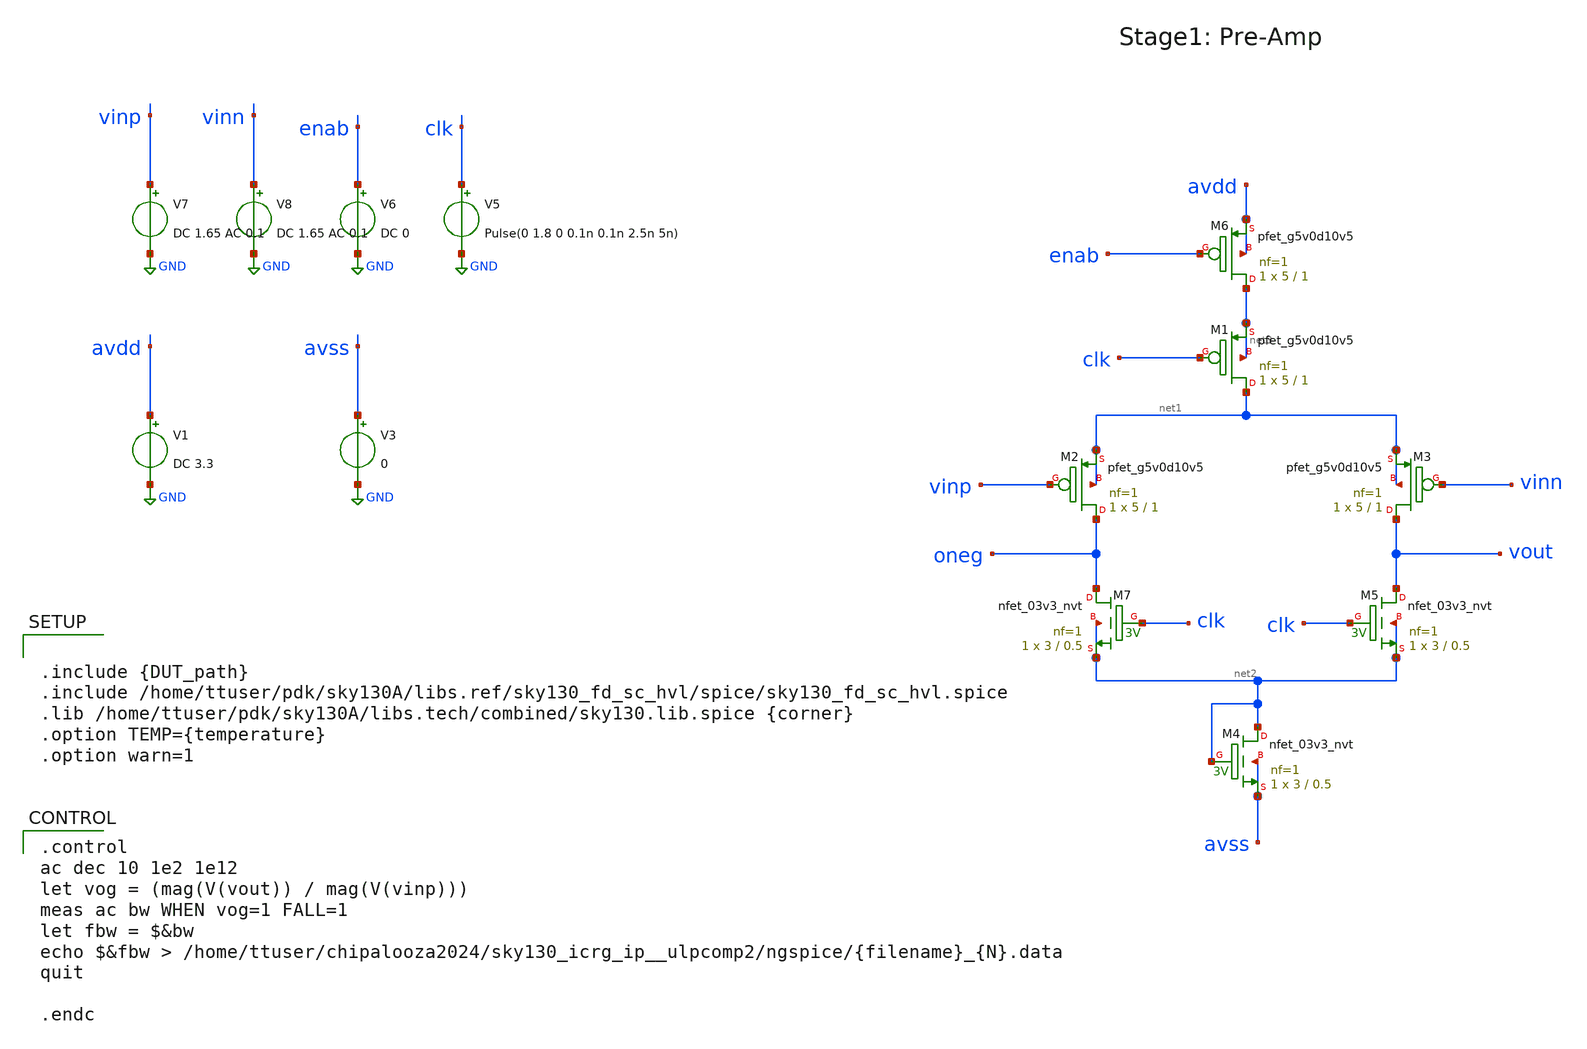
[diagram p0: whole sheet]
** sch_path: cace/fbw.sch
**.subckt fbw
XM1 net1 clk net3 net3 sky130_fd_pr__pfet_g5v0d10v5 L=1 W=5 nf=1 ad='int((nf+1)/2) * W/nf * 0.29' as='int((nf+2)/2) * W/nf * 0.29'
+ pd='2*int((nf+1)/2) * (W/nf + 0.29)' ps='2*int((nf+2)/2) * (W/nf + 0.29)' nrd='0.29 / W' nrs='0.29 / W'
+ sa=0 sb=0 sd=0 mult=1 m=1
XM2 oneg vinp net1 net1 sky130_fd_pr__pfet_g5v0d10v5 L=1 W=5 nf=1 ad='int((nf+1)/2) * W/nf * 0.29' as='int((nf+2)/2) * W/nf * 0.29'
+ pd='2*int((nf+1)/2) * (W/nf + 0.29)' ps='2*int((nf+2)/2) * (W/nf + 0.29)' nrd='0.29 / W' nrs='0.29 / W'
+ sa=0 sb=0 sd=0 mult=1 m=1
XM3 vout vinn net1 net1 sky130_fd_pr__pfet_g5v0d10v5 L=1 W=5 nf=1 ad='int((nf+1)/2) * W/nf * 0.29' as='int((nf+2)/2) * W/nf * 0.29'
+ pd='2*int((nf+1)/2) * (W/nf + 0.29)' ps='2*int((nf+2)/2) * (W/nf + 0.29)' nrd='0.29 / W' nrs='0.29 / W'
+ sa=0 sb=0 sd=0 mult=1 m=1
XM7 oneg clk net2 net2 sky130_fd_pr__nfet_03v3_nvt L=0.5 W=3 nf=1 ad='int((nf+1)/2) * W/nf * 0.29' as='int((nf+2)/2) * W/nf * 0.29'
+ pd='2*int((nf+1)/2) * (W/nf + 0.29)' ps='2*int((nf+2)/2) * (W/nf + 0.29)' nrd='0.29 / W' nrs='0.29 / W'
+ sa=0 sb=0 sd=0 mult=1 m=1
XM5 vout clk net2 net2 sky130_fd_pr__nfet_03v3_nvt L=0.5 W=3 nf=1 ad='int((nf+1)/2) * W/nf * 0.29' as='int((nf+2)/2) * W/nf * 0.29'
+ pd='2*int((nf+1)/2) * (W/nf + 0.29)' ps='2*int((nf+2)/2) * (W/nf + 0.29)' nrd='0.29 / W' nrs='0.29 / W'
+ sa=0 sb=0 sd=0 mult=1 m=1
XM4 net2 net2 avss avss sky130_fd_pr__nfet_03v3_nvt L=0.5 W=3 nf=1 ad='int((nf+1)/2) * W/nf * 0.29' as='int((nf+2)/2) * W/nf * 0.29'
+ pd='2*int((nf+1)/2) * (W/nf + 0.29)' ps='2*int((nf+2)/2) * (W/nf + 0.29)' nrd='0.29 / W' nrs='0.29 / W'
+ sa=0 sb=0 sd=0 mult=1 m=1
V1 avdd GND DC 3.3
V3 avss GND 0
V5 clk GND Pulse(0 1.8 0 0.1n 0.1n 2.5n 5n)
V6 enab GND DC 0
V7 vinp GND DC 1.65 AC 0.1
V8 vinn GND DC 1.65 AC 0.1
XM6 net3 enab avdd avdd sky130_fd_pr__pfet_g5v0d10v5 L=1 W=5 nf=1 ad='int((nf+1)/2) * W/nf * 0.29' as='int((nf+2)/2) * W/nf * 0.29'
+ pd='2*int((nf+1)/2) * (W/nf + 0.29)' ps='2*int((nf+2)/2) * (W/nf + 0.29)' nrd='0.29 / W' nrs='0.29 / W'
+ sa=0 sb=0 sd=0 mult=1 m=1
**** begin user architecture code


.include {DUT_path}
.include /home/ttuser/pdk/sky130A/libs.ref/sky130_fd_sc_hvl/spice/sky130_fd_sc_hvl.spice
.lib /home/ttuser/pdk/sky130A/libs.tech/combined/sky130.lib.spice {corner}
.option TEMP={temperature}
.option warn=1


.control
ac dec 10 1e2 1e12
let vog = (mag(V(vout)) / mag(V(vinp)))
meas ac bw WHEN vog=1 FALL=1
let fbw = $&bw
echo $&fbw > /home/ttuser/chipalooza2024/sky130_icrg_ip__ulpcomp2/ngspice/{filename}_{N}.data
quit

.endc

**** end user architecture code
**.ends
.GLOBAL GND
.end
